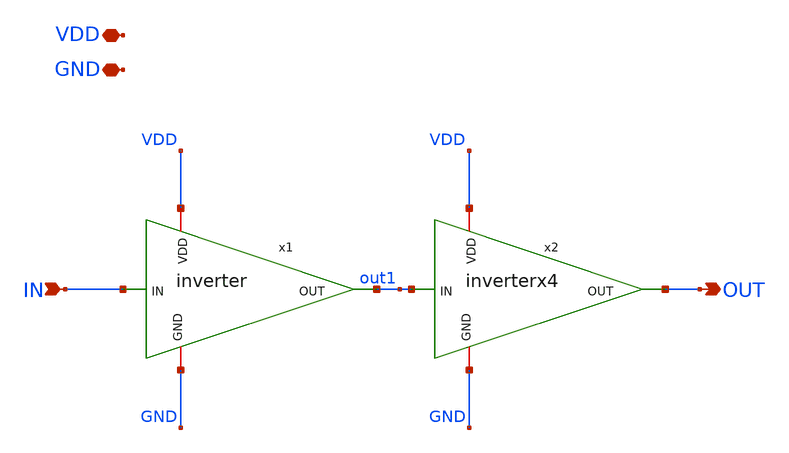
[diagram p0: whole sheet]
** sch_path: 03_magic_layout/soluzioni/lab03/xschem/buffer.sch
**.subckt buffer IN OUT VDD GND
*.ipin IN
*.opin OUT
*.iopin VDD
*.iopin GND
x1 VDD IN out1 GND inverter
x2 VDD out1 OUT GND inverterx4
**.ends
.end
